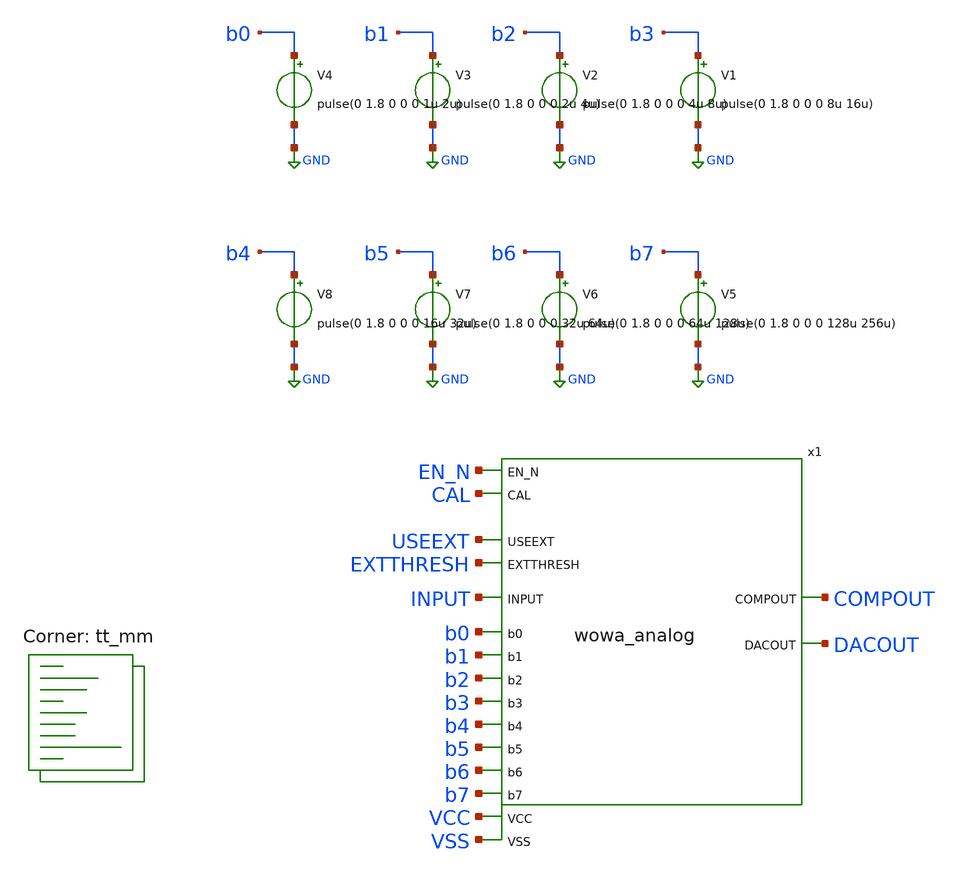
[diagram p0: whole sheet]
** sch_path: xschem/tb_wowa_analog.sch
**.subckt tb_wowa_analog
V1 b3 GND pulse(0 1.8 0 0 0 8u 16u)
V2 b2 GND pulse(0 1.8 0 0 0 4u 8u)
V3 b1 GND pulse(0 1.8 0 0 0 2u 4u)
V4 b0 GND pulse(0 1.8 0 0 0 1u 2u)
V5 b7 GND pulse(0 1.8 0 0 0 128u 256u)
V6 b6 GND pulse(0 1.8 0 0 0 64u 128u)
V7 b5 GND pulse(0 1.8 0 0 0 32u 64u)
V8 b4 GND pulse(0 1.8 0 0 0 16u 32u)
x1 VCC VSS USEEXT EN_N EXTTHRESH CAL COMPOUT INPUT b0 b1 b2 b3 b4 b5 b6 b7 DACOUT wowa_analog
**** begin user architecture code
.lib $::SKYWATER_MODELS/sky130.lib.spice tt_mm


** this experimental option enables mos model bin
** selection based on W/NF instead of W
.option chgtol=4e-16 method=gear

.param VCCGAUSS = agauss(1.8, 0.05, 1)
.param VCC = 'VCCGAUSS'
** use following line to remove VCC variations
* .param VCC = 1.8
.param VDLGAUSS = agauss(0.9, 0.23, 1)
.param VDL = VDLGAUSS
** use following line to remove input common mode variations
* .param VDL =  0.9
.param TEMPGAUSS = agauss(40, 30, 1)
.option temp = 'TEMPGAUSS'
** use following line to remove temperature variations
* .option temp = 25
.param DELTA = 0.002

.include stimuli_tb_wowa_analog.cir

.control
  setseed  8
  reset
  let run = 1
  save all
  op
  write tb_wowa_analog.raw
  reset
  set appendwrite
  dowhile run < = 5
    save all
    tran 50n 150u uic
    write tb_wowa_analog.raw
    let run = run + 1
    reset
  end
  quit 0
.endc


**** end user architecture code
**.ends
.GLOBAL GND
.end
